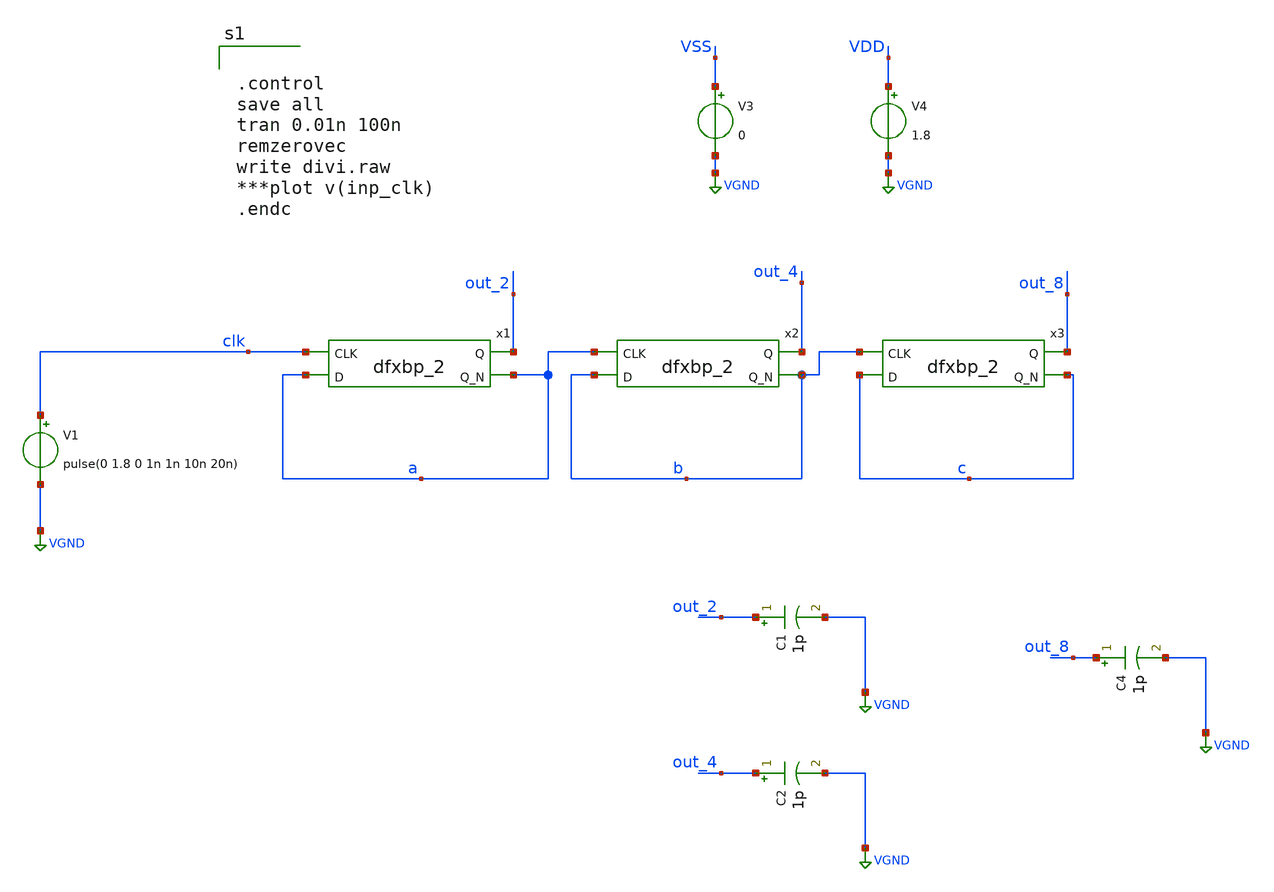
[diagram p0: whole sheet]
** sch_path: xschem/divi.sch
.lib $::SKYWATER_MODELS/sky130.lib.spice tt
.include $::SKYWATER_STDCELLS/sky130_fd_sc_hd.spice

**.subckt divi
x1 clk a VSS VSS VDD VDD out_2 a sky130_fd_sc_hd__dfxbp_2
C4 out_8 VGND 1p m=1
C1 out_2 VGND 1p m=1
C2 out_4 VGND 1p m=1
V3 VSS VGND 0
x2 a b VSS VSS VDD VDD out_4 b sky130_fd_sc_hd__dfxbp_2
x3 b c VSS VSS VDD VDD out_8 c sky130_fd_sc_hd__dfxbp_2
V1 clk VGND pulse(0 1.8 0 1n 1n 10n 20n)
V4 VDD VGND 1.8
**** begin user architecture code


.control
save all
tran 0.01n 100n
remzerovec
write divi.raw
***plot v(inp_clk)
.endc


**** end user architecture code
**.ends
.GLOBAL VGND
.end
